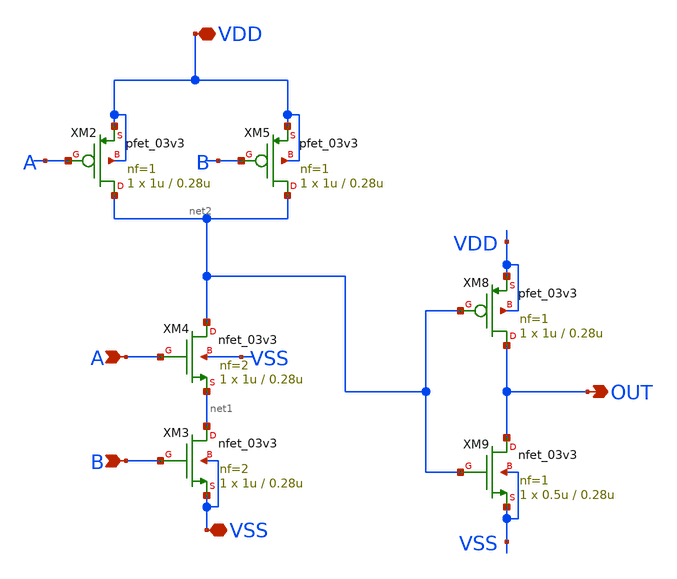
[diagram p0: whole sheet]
** sch_path: SCOP_INPUT_AND_MUX_PAKISTAN_03/Xschem/Logic_Gates/AND_2_Input.sch
**.subckt AND_2_Input VDD VSS A B OUT
*.iopin VDD
*.iopin VSS
*.ipin A
*.ipin B
*.opin OUT
XM2 net2 A VDD VDD pfet_03v3 L=0.28u W=1u nf=1 ad='int((nf+1)/2) * W/nf * 0.18u' as='int((nf+2)/2) * W/nf * 0.18u'
+ pd='2*int((nf+1)/2) * (W/nf + 0.18u)' ps='2*int((nf+2)/2) * (W/nf + 0.18u)' nrd='0.18u / W' nrs='0.18u / W'
+ sa=0 sb=0 sd=0 m=1
XM3 net1 B VSS VSS nfet_03v3 L=0.28u W=1u nf=2 ad='int((nf+1)/2) * W/nf * 0.18u' as='int((nf+2)/2) * W/nf * 0.18u'
+ pd='2*int((nf+1)/2) * (W/nf + 0.18u)' ps='2*int((nf+2)/2) * (W/nf + 0.18u)' nrd='0.18u / W' nrs='0.18u / W'
+ sa=0 sb=0 sd=0 m=1
XM4 net2 A net1 VSS nfet_03v3 L=0.28u W=1u nf=2 ad='int((nf+1)/2) * W/nf * 0.18u' as='int((nf+2)/2) * W/nf * 0.18u'
+ pd='2*int((nf+1)/2) * (W/nf + 0.18u)' ps='2*int((nf+2)/2) * (W/nf + 0.18u)' nrd='0.18u / W' nrs='0.18u / W'
+ sa=0 sb=0 sd=0 m=1
XM5 net2 B VDD VDD pfet_03v3 L=0.28u W=1u nf=1 ad='int((nf+1)/2) * W/nf * 0.18u' as='int((nf+2)/2) * W/nf * 0.18u'
+ pd='2*int((nf+1)/2) * (W/nf + 0.18u)' ps='2*int((nf+2)/2) * (W/nf + 0.18u)' nrd='0.18u / W' nrs='0.18u / W'
+ sa=0 sb=0 sd=0 m=1
XM8 OUT net2 VDD VDD pfet_03v3 L=0.28u W=1u nf=1 ad='int((nf+1)/2) * W/nf * 0.18u' as='int((nf+2)/2) * W/nf * 0.18u'
+ pd='2*int((nf+1)/2) * (W/nf + 0.18u)' ps='2*int((nf+2)/2) * (W/nf + 0.18u)' nrd='0.18u / W' nrs='0.18u / W'
+ sa=0 sb=0 sd=0 m=1
XM9 OUT net2 VSS VSS nfet_03v3 L=0.28u W=0.5u nf=1 ad='int((nf+1)/2) * W/nf * 0.18u' as='int((nf+2)/2) * W/nf * 0.18u'
+ pd='2*int((nf+1)/2) * (W/nf + 0.18u)' ps='2*int((nf+2)/2) * (W/nf + 0.18u)' nrd='0.18u / W' nrs='0.18u / W'
+ sa=0 sb=0 sd=0 m=1
**.ends
.end
